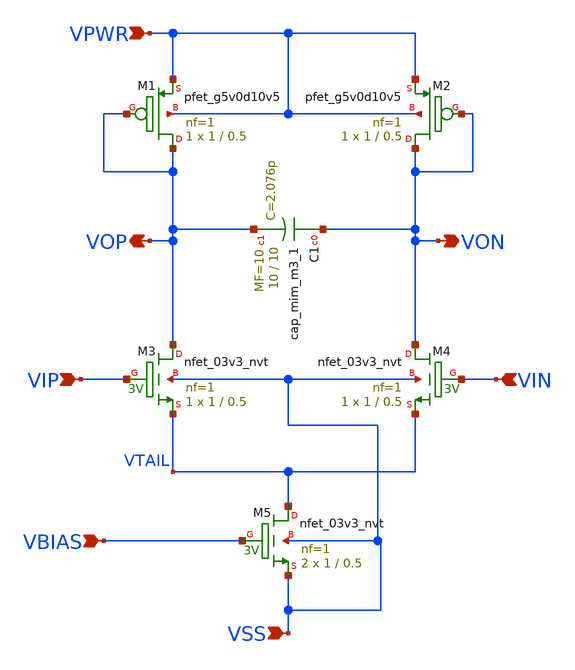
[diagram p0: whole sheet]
** sch_path: xschem/gm-c_filter/gm-c-filter_0.sch
**.subckt gm-c-filter_0 VBIAS VIP VPWR VIN VSS VON VOP
*.ipin VBIAS
*.ipin VIP
*.ipin VPWR
*.ipin VIN
*.ipin VSS
*.opin VON
*.opin VOP
XM1 VOP VOP VPWR VPWR sky130_fd_pr__pfet_g5v0d10v5 L=0.5 W=1 nf=1 ad='int((nf+1)/2) * W/nf * 0.29' as='int((nf+2)/2) * W/nf * 0.29'
+ pd='2*int((nf+1)/2) * (W/nf + 0.29)' ps='2*int((nf+2)/2) * (W/nf + 0.29)' nrd='0.29 / W' nrs='0.29 / W'
+ sa=0 sb=0 sd=0 mult=1 m=1
XM2 VON VON VPWR VPWR sky130_fd_pr__pfet_g5v0d10v5 L=0.5 W=1 nf=1 ad='int((nf+1)/2) * W/nf * 0.29' as='int((nf+2)/2) * W/nf * 0.29'
+ pd='2*int((nf+1)/2) * (W/nf + 0.29)' ps='2*int((nf+2)/2) * (W/nf + 0.29)' nrd='0.29 / W' nrs='0.29 / W'
+ sa=0 sb=0 sd=0 mult=1 m=1
XM3 VOP VIP VTAIL VSS sky130_fd_pr__nfet_03v3_nvt L=0.5 W=1 nf=1 ad='int((nf+1)/2) * W/nf * 0.29' as='int((nf+2)/2) * W/nf * 0.29'
+ pd='2*int((nf+1)/2) * (W/nf + 0.29)' ps='2*int((nf+2)/2) * (W/nf + 0.29)' nrd='0.29 / W' nrs='0.29 / W'
+ sa=0 sb=0 sd=0 mult=1 m=1
XM4 VON VIN VTAIL VSS sky130_fd_pr__nfet_03v3_nvt L=0.5 W=1 nf=1 ad='int((nf+1)/2) * W/nf * 0.29' as='int((nf+2)/2) * W/nf * 0.29'
+ pd='2*int((nf+1)/2) * (W/nf + 0.29)' ps='2*int((nf+2)/2) * (W/nf + 0.29)' nrd='0.29 / W' nrs='0.29 / W'
+ sa=0 sb=0 sd=0 mult=1 m=1
XC1 VON VOP sky130_fd_pr__cap_mim_m3_1 W=10 L=10 MF=10 m=10
XM5 VTAIL VBIAS VSS VSS sky130_fd_pr__nfet_03v3_nvt L=0.5 W=1 nf=1 ad='int((nf+1)/2) * W/nf * 0.29' as='int((nf+2)/2) * W/nf * 0.29'
+ pd='2*int((nf+1)/2) * (W/nf + 0.29)' ps='2*int((nf+2)/2) * (W/nf + 0.29)' nrd='0.29 / W' nrs='0.29 / W'
+ sa=0 sb=0 sd=0 mult=2 m=2
**.ends
.end
